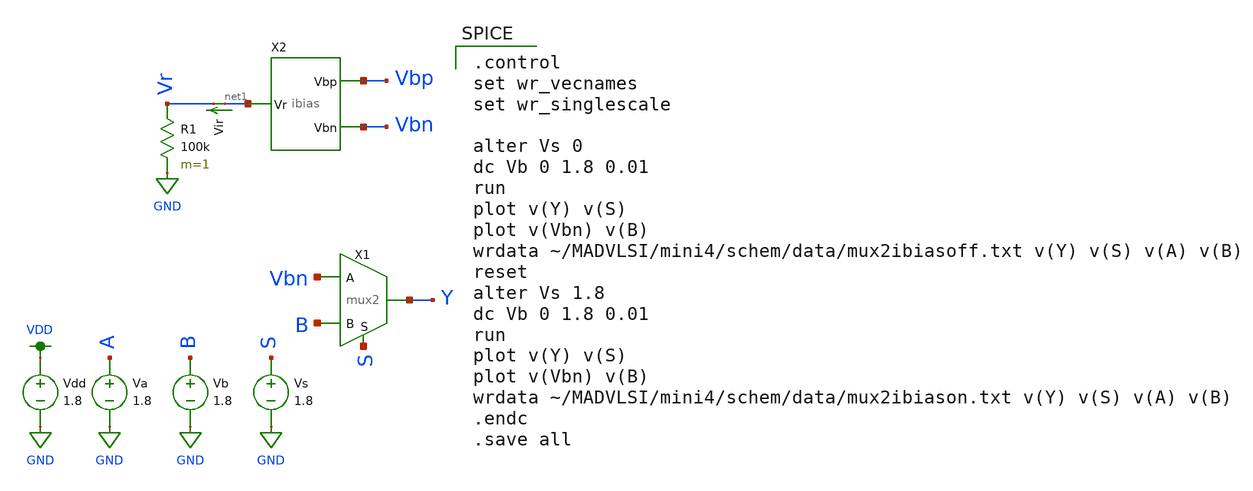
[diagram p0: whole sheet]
** sch_path: mini4/schem/mux2ibias_test.sch
**.subckt mux2ibias_test
X1 Y Vbn B S mux2
Va A GND 1.8
Vb B GND 1.8
Vdd VDD GND 1.8
Vs S GND 1.8
X2 net1 Vbn Vbp ibias
R1 Vr GND 100k m=1
Vir net1 Vr 0
.save i(vir)
**** begin user architecture code

.option wnflag=1
.param MC_SWITCH=0.0
.lib ~/skywater/skywater-pdk/libraries/sky130_fd_pr_ngspice/latest/models/sky130.lib.spice tt


.control
set wr_vecnames
set wr_singlescale

alter Vs 0
dc Vb 0 1.8 0.01
run
plot v(Y) v(S)
plot v(Vbn) v(B)
wrdata ~/MADVLSI/mini4/schem/data/mux2ibiasoff.txt v(Y) v(S) v(A) v(B)
reset
alter Vs 1.8
dc Vb 0 1.8 0.01
run
plot v(Y) v(S)
plot v(Vbn) v(B)
wrdata ~/MADVLSI/mini4/schem/data/mux2ibiason.txt v(Y) v(S) v(A) v(B)
.endc
.save all


**** end user architecture code
**.ends
.GLOBAL GND
.GLOBAL VDD
.end
